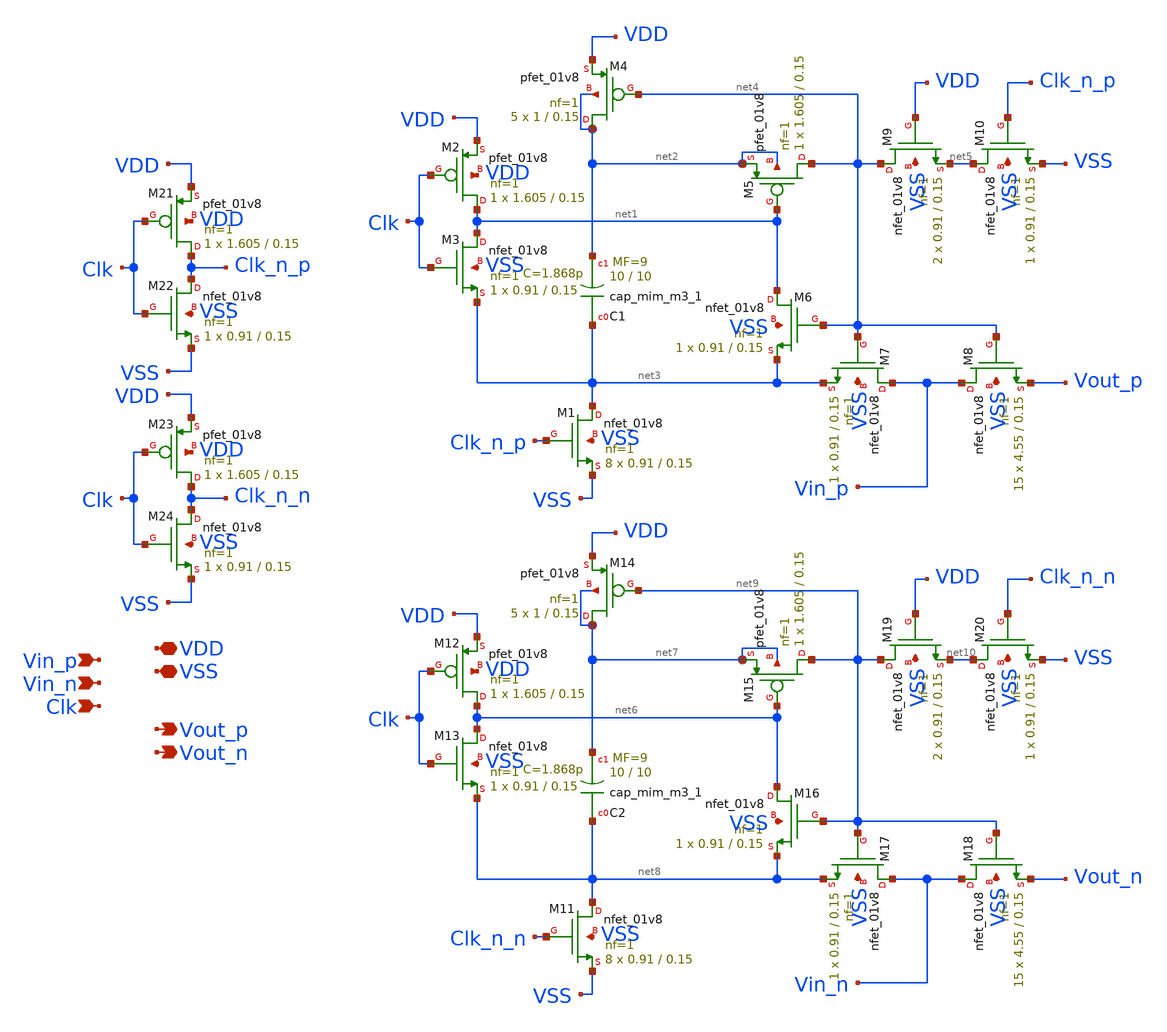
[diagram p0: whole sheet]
** sch_path: xschem/src/bootstrapped_sampling_switch/bootstrapped_sampling_switch.sch
**.subckt bootstrapped_sampling_switch VDD Vin_p Vout_p VSS Vout_n Vin_n Clk
*.iopin VDD
*.ipin Vin_p
*.opin Vout_p
*.iopin VSS
*.opin Vout_n
*.ipin Vin_n
*.ipin Clk
XM1 net3 Clk_n_p VSS VSS sky130_fd_pr__nfet_01v8 L=0.15 W=0.91 nf=1 ad='int((nf+1)/2) * W/nf * 0.29'
+ as='int((nf+2)/2) * W/nf * 0.29' pd='2*int((nf+1)/2) * (W/nf + 0.29)' ps='2*int((nf+2)/2) * (W/nf + 0.29)'
+ nrd='0.29 / W' nrs='0.29 / W' sa=0 sb=0 sd=0 mult=8 m=8
XM2 net1 Clk VDD VDD sky130_fd_pr__pfet_01v8 L=0.15 W=1.605 nf=1 ad='int((nf+1)/2) * W/nf * 0.29' as='int((nf+2)/2) * W/nf * 0.29'
+ pd='2*int((nf+1)/2) * (W/nf + 0.29)' ps='2*int((nf+2)/2) * (W/nf + 0.29)' nrd='0.29 / W' nrs='0.29 / W'
+ sa=0 sb=0 sd=0 mult=1 m=1
XM3 net1 Clk net3 VSS sky130_fd_pr__nfet_01v8 L=0.15 W=0.91 nf=1 ad='int((nf+1)/2) * W/nf * 0.29' as='int((nf+2)/2) * W/nf * 0.29'
+ pd='2*int((nf+1)/2) * (W/nf + 0.29)' ps='2*int((nf+2)/2) * (W/nf + 0.29)' nrd='0.29 / W' nrs='0.29 / W'
+ sa=0 sb=0 sd=0 mult=1 m=1
XC1 net3 net2 sky130_fd_pr__cap_mim_m3_1 W=10 L=10 MF=9 m=9
XM4 net2 net4 VDD net2 sky130_fd_pr__pfet_01v8 L=0.15 W=1 nf=1 ad='int((nf+1)/2) * W/nf * 0.29' as='int((nf+2)/2) * W/nf * 0.29'
+ pd='2*int((nf+1)/2) * (W/nf + 0.29)' ps='2*int((nf+2)/2) * (W/nf + 0.29)' nrd='0.29 / W' nrs='0.29 / W'
+ sa=0 sb=0 sd=0 mult=5 m=5
XM5 net4 net1 net2 net2 sky130_fd_pr__pfet_01v8 L=0.15 W=1.605 nf=1 ad='int((nf+1)/2) * W/nf * 0.29'
+ as='int((nf+2)/2) * W/nf * 0.29' pd='2*int((nf+1)/2) * (W/nf + 0.29)' ps='2*int((nf+2)/2) * (W/nf + 0.29)'
+ nrd='0.29 / W' nrs='0.29 / W' sa=0 sb=0 sd=0 mult=1 m=1
XM6 net1 net4 net3 VSS sky130_fd_pr__nfet_01v8 L=0.15 W=0.91 nf=1 ad='int((nf+1)/2) * W/nf * 0.29' as='int((nf+2)/2) * W/nf * 0.29'
+ pd='2*int((nf+1)/2) * (W/nf + 0.29)' ps='2*int((nf+2)/2) * (W/nf + 0.29)' nrd='0.29 / W' nrs='0.29 / W'
+ sa=0 sb=0 sd=0 mult=1 m=1
XM7 Vin_p net4 net3 VSS sky130_fd_pr__nfet_01v8 L=0.15 W=0.91 nf=1 ad='int((nf+1)/2) * W/nf * 0.29' as='int((nf+2)/2) * W/nf * 0.29'
+ pd='2*int((nf+1)/2) * (W/nf + 0.29)' ps='2*int((nf+2)/2) * (W/nf + 0.29)' nrd='0.29 / W' nrs='0.29 / W'
+ sa=0 sb=0 sd=0 mult=1 m=1
XM8 Vin_p net4 Vout_p VSS sky130_fd_pr__nfet_01v8 L=0.15 W=4.55 nf=1 ad='int((nf+1)/2) * W/nf * 0.29'
+ as='int((nf+2)/2) * W/nf * 0.29' pd='2*int((nf+1)/2) * (W/nf + 0.29)' ps='2*int((nf+2)/2) * (W/nf + 0.29)'
+ nrd='0.29 / W' nrs='0.29 / W' sa=0 sb=0 sd=0 mult=15 m=15
XM9 net4 VDD net5 VSS sky130_fd_pr__nfet_01v8 L=0.15 W=0.91 nf=1 ad='int((nf+1)/2) * W/nf * 0.29' as='int((nf+2)/2) * W/nf * 0.29'
+ pd='2*int((nf+1)/2) * (W/nf + 0.29)' ps='2*int((nf+2)/2) * (W/nf + 0.29)' nrd='0.29 / W' nrs='0.29 / W'
+ sa=0 sb=0 sd=0 mult=2 m=2
XM10 net5 Clk_n_p VSS VSS sky130_fd_pr__nfet_01v8 L=0.15 W=0.91 nf=1 ad='int((nf+1)/2) * W/nf * 0.29'
+ as='int((nf+2)/2) * W/nf * 0.29' pd='2*int((nf+1)/2) * (W/nf + 0.29)' ps='2*int((nf+2)/2) * (W/nf + 0.29)'
+ nrd='0.29 / W' nrs='0.29 / W' sa=0 sb=0 sd=0 mult=1 m=1
XM11 net8 Clk_n_n VSS VSS sky130_fd_pr__nfet_01v8 L=0.15 W=0.91 nf=1 ad='int((nf+1)/2) * W/nf * 0.29'
+ as='int((nf+2)/2) * W/nf * 0.29' pd='2*int((nf+1)/2) * (W/nf + 0.29)' ps='2*int((nf+2)/2) * (W/nf + 0.29)'
+ nrd='0.29 / W' nrs='0.29 / W' sa=0 sb=0 sd=0 mult=8 m=8
XM12 net6 Clk VDD VDD sky130_fd_pr__pfet_01v8 L=0.15 W=1.605 nf=1 ad='int((nf+1)/2) * W/nf * 0.29' as='int((nf+2)/2) * W/nf * 0.29'
+ pd='2*int((nf+1)/2) * (W/nf + 0.29)' ps='2*int((nf+2)/2) * (W/nf + 0.29)' nrd='0.29 / W' nrs='0.29 / W'
+ sa=0 sb=0 sd=0 mult=1 m=1
XM13 net6 Clk net8 VSS sky130_fd_pr__nfet_01v8 L=0.15 W=0.91 nf=1 ad='int((nf+1)/2) * W/nf * 0.29' as='int((nf+2)/2) * W/nf * 0.29'
+ pd='2*int((nf+1)/2) * (W/nf + 0.29)' ps='2*int((nf+2)/2) * (W/nf + 0.29)' nrd='0.29 / W' nrs='0.29 / W'
+ sa=0 sb=0 sd=0 mult=1 m=1
XC2 net8 net7 sky130_fd_pr__cap_mim_m3_1 W=10 L=10 MF=9 m=9
XM14 net7 net9 VDD net7 sky130_fd_pr__pfet_01v8 L=0.15 W=1 nf=1 ad='int((nf+1)/2) * W/nf * 0.29' as='int((nf+2)/2) * W/nf * 0.29'
+ pd='2*int((nf+1)/2) * (W/nf + 0.29)' ps='2*int((nf+2)/2) * (W/nf + 0.29)' nrd='0.29 / W' nrs='0.29 / W'
+ sa=0 sb=0 sd=0 mult=5 m=5
XM15 net9 net6 net7 net7 sky130_fd_pr__pfet_01v8 L=0.15 W=1.605 nf=1 ad='int((nf+1)/2) * W/nf * 0.29'
+ as='int((nf+2)/2) * W/nf * 0.29' pd='2*int((nf+1)/2) * (W/nf + 0.29)' ps='2*int((nf+2)/2) * (W/nf + 0.29)'
+ nrd='0.29 / W' nrs='0.29 / W' sa=0 sb=0 sd=0 mult=1 m=1
XM16 net6 net9 net8 VSS sky130_fd_pr__nfet_01v8 L=0.15 W=0.91 nf=1 ad='int((nf+1)/2) * W/nf * 0.29' as='int((nf+2)/2) * W/nf * 0.29'
+ pd='2*int((nf+1)/2) * (W/nf + 0.29)' ps='2*int((nf+2)/2) * (W/nf + 0.29)' nrd='0.29 / W' nrs='0.29 / W'
+ sa=0 sb=0 sd=0 mult=1 m=1
XM17 Vin_n net9 net8 VSS sky130_fd_pr__nfet_01v8 L=0.15 W=0.91 nf=1 ad='int((nf+1)/2) * W/nf * 0.29'
+ as='int((nf+2)/2) * W/nf * 0.29' pd='2*int((nf+1)/2) * (W/nf + 0.29)' ps='2*int((nf+2)/2) * (W/nf + 0.29)'
+ nrd='0.29 / W' nrs='0.29 / W' sa=0 sb=0 sd=0 mult=1 m=1
XM18 Vin_n net9 Vout_n VSS sky130_fd_pr__nfet_01v8 L=0.15 W=4.55 nf=1 ad='int((nf+1)/2) * W/nf * 0.29'
+ as='int((nf+2)/2) * W/nf * 0.29' pd='2*int((nf+1)/2) * (W/nf + 0.29)' ps='2*int((nf+2)/2) * (W/nf + 0.29)'
+ nrd='0.29 / W' nrs='0.29 / W' sa=0 sb=0 sd=0 mult=15 m=15
XM19 net9 VDD net10 VSS sky130_fd_pr__nfet_01v8 L=0.15 W=0.91 nf=1 ad='int((nf+1)/2) * W/nf * 0.29' as='int((nf+2)/2) * W/nf * 0.29'
+ pd='2*int((nf+1)/2) * (W/nf + 0.29)' ps='2*int((nf+2)/2) * (W/nf + 0.29)' nrd='0.29 / W' nrs='0.29 / W'
+ sa=0 sb=0 sd=0 mult=2 m=2
XM20 net10 Clk_n_n VSS VSS sky130_fd_pr__nfet_01v8 L=0.15 W=0.91 nf=1 ad='int((nf+1)/2) * W/nf * 0.29'
+ as='int((nf+2)/2) * W/nf * 0.29' pd='2*int((nf+1)/2) * (W/nf + 0.29)' ps='2*int((nf+2)/2) * (W/nf + 0.29)'
+ nrd='0.29 / W' nrs='0.29 / W' sa=0 sb=0 sd=0 mult=1 m=1
XM21 Clk_n_p Clk VDD VDD sky130_fd_pr__pfet_01v8 L=0.15 W=1.605 nf=1 ad='int((nf+1)/2) * W/nf * 0.29'
+ as='int((nf+2)/2) * W/nf * 0.29' pd='2*int((nf+1)/2) * (W/nf + 0.29)' ps='2*int((nf+2)/2) * (W/nf + 0.29)'
+ nrd='0.29 / W' nrs='0.29 / W' sa=0 sb=0 sd=0 mult=1 m=1
XM22 Clk_n_p Clk VSS VSS sky130_fd_pr__nfet_01v8 L=0.15 W=0.91 nf=1 ad='int((nf+1)/2) * W/nf * 0.29'
+ as='int((nf+2)/2) * W/nf * 0.29' pd='2*int((nf+1)/2) * (W/nf + 0.29)' ps='2*int((nf+2)/2) * (W/nf + 0.29)'
+ nrd='0.29 / W' nrs='0.29 / W' sa=0 sb=0 sd=0 mult=1 m=1
XM23 Clk_n_n Clk VDD VDD sky130_fd_pr__pfet_01v8 L=0.15 W=1.605 nf=1 ad='int((nf+1)/2) * W/nf * 0.29'
+ as='int((nf+2)/2) * W/nf * 0.29' pd='2*int((nf+1)/2) * (W/nf + 0.29)' ps='2*int((nf+2)/2) * (W/nf + 0.29)'
+ nrd='0.29 / W' nrs='0.29 / W' sa=0 sb=0 sd=0 mult=1 m=1
XM24 Clk_n_n Clk VSS VSS sky130_fd_pr__nfet_01v8 L=0.15 W=0.91 nf=1 ad='int((nf+1)/2) * W/nf * 0.29'
+ as='int((nf+2)/2) * W/nf * 0.29' pd='2*int((nf+1)/2) * (W/nf + 0.29)' ps='2*int((nf+2)/2) * (W/nf + 0.29)'
+ nrd='0.29 / W' nrs='0.29 / W' sa=0 sb=0 sd=0 mult=1 m=1
**.ends
.end
